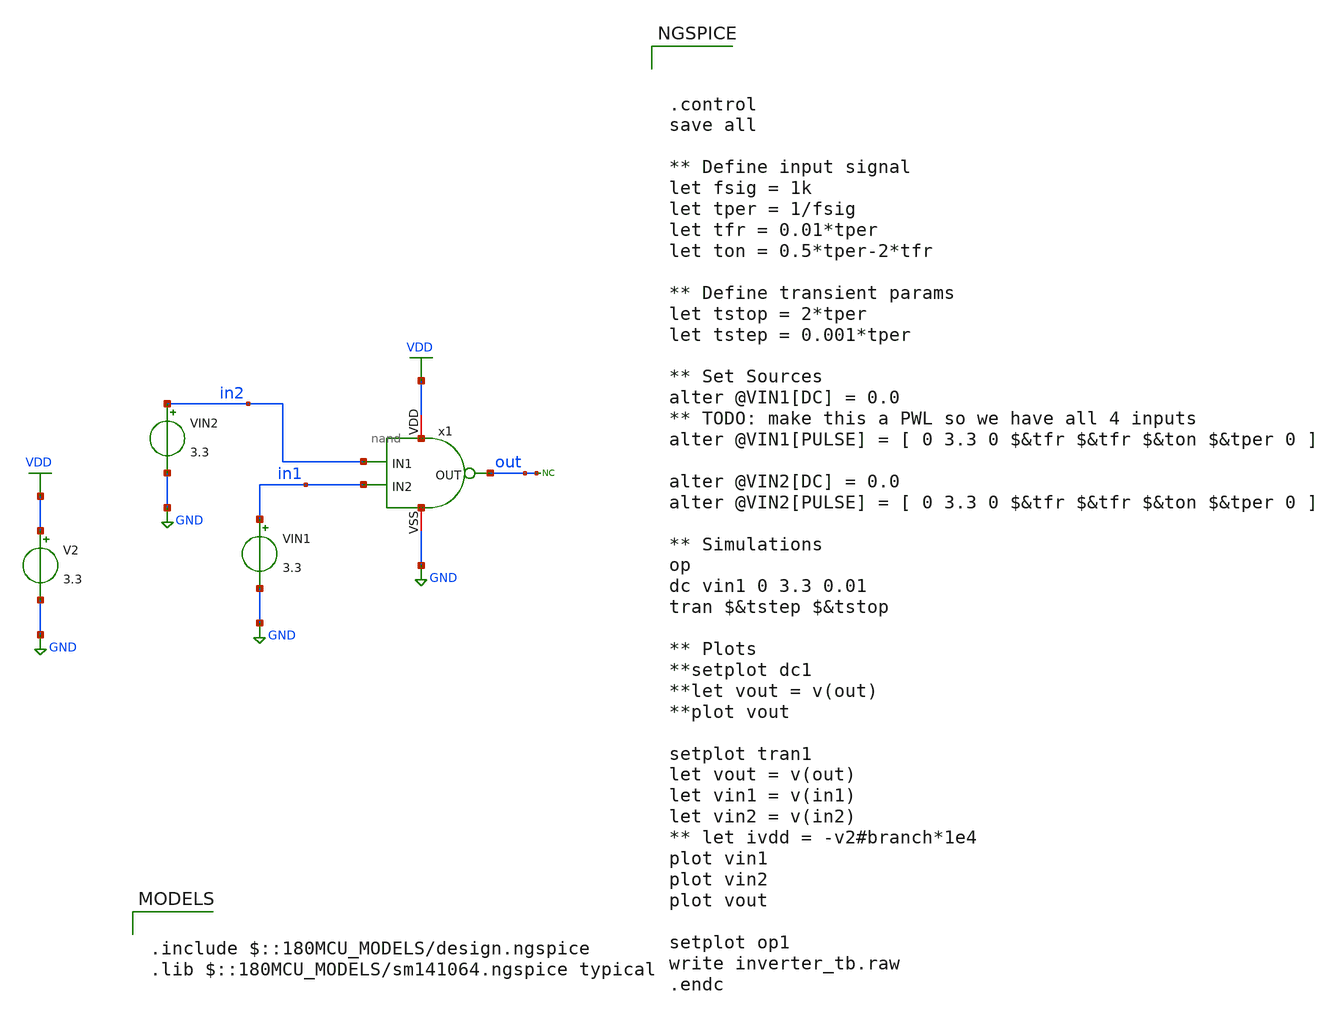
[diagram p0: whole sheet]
** sch_path: designs/libs/nand/nand_tb.sch
**.subckt nand_tb
x1 VDD out in2 in1 GND nand
V2 VDD GND 3.3
VIN1 in1 GND 3.3
VIN2 in2 GND 3.3
* noconn out
**** begin user architecture code

.include $::180MCU_MODELS/design.ngspice
.lib $::180MCU_MODELS/sm141064.ngspice typical




.control
save all

** Define input signal
let fsig = 1k
let tper = 1/fsig
let tfr = 0.01*tper
let ton = 0.5*tper-2*tfr

** Define transient params
let tstop = 2*tper
let tstep = 0.001*tper

** Set Sources
alter @VIN1[DC] = 0.0
** TODO: make this a PWL so we have all 4 inputs
alter @VIN1[PULSE] = [ 0 3.3 0 $&tfr $&tfr $&ton $&tper 0 ]

alter @VIN2[DC] = 0.0
alter @VIN2[PULSE] = [ 0 3.3 0 $&tfr $&tfr $&ton $&tper 0 ]

** Simulations
op
dc vin1 0 3.3 0.01
tran $&tstep $&tstop

** Plots
**setplot dc1
**let vout = v(out)
**plot vout

setplot tran1
let vout = v(out)
let vin1 = v(in1)
let vin2 = v(in2)
** let ivdd = -v2#branch*1e4
plot vin1
plot vin2
plot vout

setplot op1
write inverter_tb.raw
.endc


**** end user architecture code
**.ends

* expanding   symbol:  libs/nand/nand.sym # of pins=5
** sym_path: designs/libs/nand/nand.sym
** sch_path: designs/libs/nand/nand.sch
.subckt nand VDD OUT IN1 IN2 VSS
*.ipin IN1
*.ipin IN2
*.opin OUT
*.iopin VDD
*.iopin VSS
XM1 OUT IN1 net1 VSS nfet_03v3 L=0.28u W=0.22u nf=1 ad='int((nf+1)/2) * W/nf * 0.18u' as='int((nf+2)/2) * W/nf * 0.18u'
+ pd='2*int((nf+1)/2) * (W/nf + 0.18u)' ps='2*int((nf+2)/2) * (W/nf + 0.18u)' nrd='0.18u / W' nrs='0.18u / W'
+ sa=0 sb=0 sd=0 m=1
XM2 net1 IN2 VSS VSS nfet_03v3 L=0.28u W=0.22u nf=1 ad='int((nf+1)/2) * W/nf * 0.18u' as='int((nf+2)/2) * W/nf * 0.18u'
+ pd='2*int((nf+1)/2) * (W/nf + 0.18u)' ps='2*int((nf+2)/2) * (W/nf + 0.18u)' nrd='0.18u / W' nrs='0.18u / W'
+ sa=0 sb=0 sd=0 m=1
XM3 OUT IN1 VDD VDD pfet_03v3 L=0.28u W=0.22u nf=1 ad='int((nf+1)/2) * W/nf * 0.18u' as='int((nf+2)/2) * W/nf * 0.18u'
+ pd='2*int((nf+1)/2) * (W/nf + 0.18u)' ps='2*int((nf+2)/2) * (W/nf + 0.18u)' nrd='0.18u / W' nrs='0.18u / W'
+ sa=0 sb=0 sd=0 m=1
XM4 OUT IN2 VDD VDD pfet_03v3 L=0.28u W=0.22u nf=1 ad='int((nf+1)/2) * W/nf * 0.18u' as='int((nf+2)/2) * W/nf * 0.18u'
+ pd='2*int((nf+1)/2) * (W/nf + 0.18u)' ps='2*int((nf+2)/2) * (W/nf + 0.18u)' nrd='0.18u / W' nrs='0.18u / W'
+ sa=0 sb=0 sd=0 m=1
.ends

.GLOBAL GND
.GLOBAL VDD
.end
